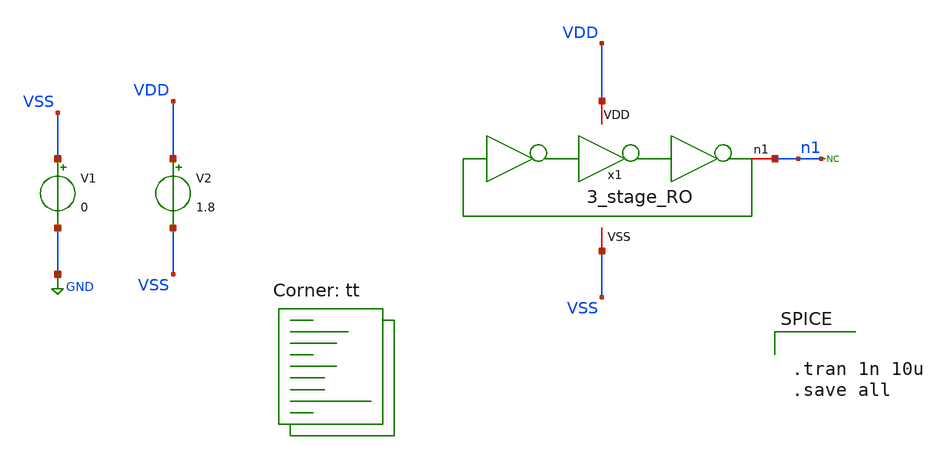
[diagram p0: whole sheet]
** sch_path: Modulo_Analogico/Lab2/3_stage_RO_tb_tran.sch
**.subckt 3_stage_RO_tb_tran
V1 VSS GND 0
V2 VDD VSS 1.8
* noconn n1
x1 VDD VSS n1 3_stage_RO
**** begin user architecture code


.tran 1n 10u
.save all



.lib $::SKYWATER_MODELS/sky130.lib.spice tt
**** end user architecture code
**.ends

* expanding   symbol:
*+  /foss/designs/Virtual_bootcamp_Circuify_ChipPractice/Modulo_Analogico/Lab2/3_stage_RO.sym # of pins=3
** sym_path: /foss/designs/Virtual_bootcamp_Circuify_ChipPractice/Modulo_Analogico/Lab2/3_stage_RO.sym
** sch_path: /foss/designs/Virtual_bootcamp_Circuify_ChipPractice/Modulo_Analogico/Lab2/3_stage_RO.sch
.subckt 3_stage_RO VDD VSS n1
*.iopin VDD
*.iopin VSS
*.iopin n1
x1 n1 VDD VSS n2 inverter
x2 n2 VDD VSS n3 inverter
x3 n3 VDD VSS n1 inverter
.ends

.GLOBAL GND
.end
